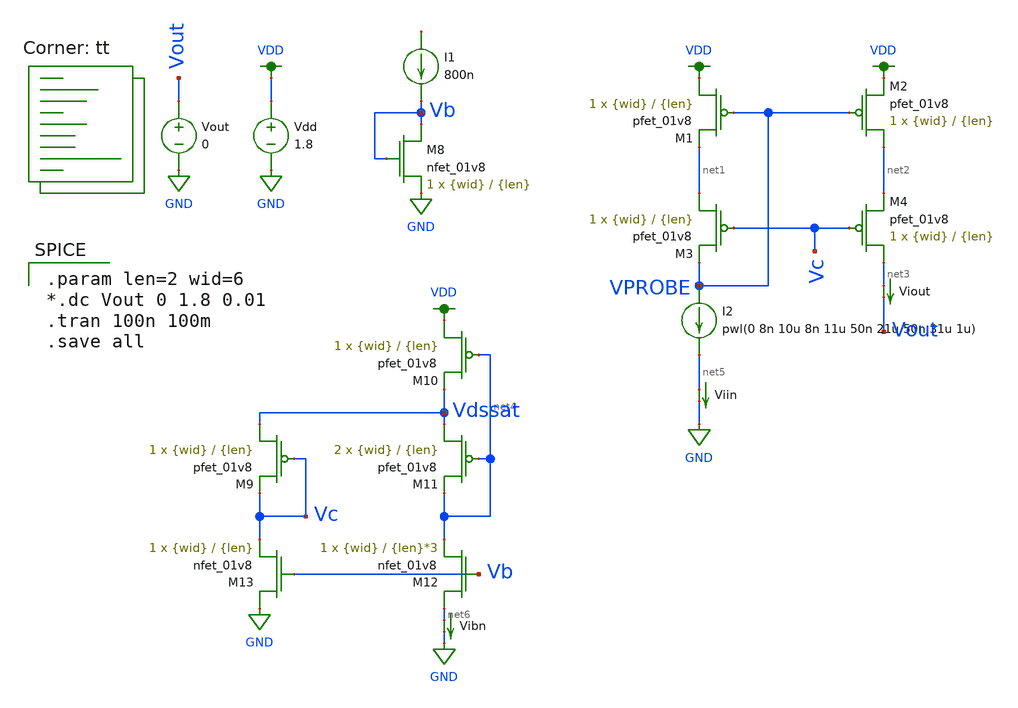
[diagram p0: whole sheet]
** sch_path: mp3/mirror_v2_tb.sch
**.subckt mirror_v2_tb
XM1 VDD VPROBE net1 VDD sky130_fd_pr__pfet_01v8 L={len} W={wid} nf=1 ad='int((nf+1)/2) * W/nf * 0.29'
+ as='int((nf+2)/2) * W/nf * 0.29' pd='2*int((nf+1)/2) * (W/nf + 0.29)' ps='2*int((nf+2)/2) * (W/nf + 0.29)'
+ nrd='0.29 / W' nrs='0.29 / W' sa=0 sb=0 sd=0 mult=1 m=1
XM2 net2 VPROBE VDD VDD sky130_fd_pr__pfet_01v8 L={len} W={wid} nf=1 ad='int((nf+1)/2) * W/nf * 0.29'
+ as='int((nf+2)/2) * W/nf * 0.29' pd='2*int((nf+1)/2) * (W/nf + 0.29)' ps='2*int((nf+2)/2) * (W/nf + 0.29)'
+ nrd='0.29 / W' nrs='0.29 / W' sa=0 sb=0 sd=0 mult=1 m=1
XM3 net1 Vc VPROBE VDD sky130_fd_pr__pfet_01v8 L={len} W={wid} nf=1 ad='int((nf+1)/2) * W/nf * 0.29'
+ as='int((nf+2)/2) * W/nf * 0.29' pd='2*int((nf+1)/2) * (W/nf + 0.29)' ps='2*int((nf+2)/2) * (W/nf + 0.29)'
+ nrd='0.29 / W' nrs='0.29 / W' sa=0 sb=0 sd=0 mult=1 m=1
XM4 net3 Vc net2 VDD sky130_fd_pr__pfet_01v8 L={len} W={wid} nf=1 ad='int((nf+1)/2) * W/nf * 0.29' as='int((nf+2)/2) * W/nf * 0.29'
+ pd='2*int((nf+1)/2) * (W/nf + 0.29)' ps='2*int((nf+2)/2) * (W/nf + 0.29)' nrd='0.29 / W' nrs='0.29 / W'
+ sa=0 sb=0 sd=0 mult=1 m=1
XM8 Vb Vb GND GND sky130_fd_pr__nfet_01v8 L={len} W={wid} nf=1 ad='int((nf+1)/2) * W/nf * 0.29' as='int((nf+2)/2) * W/nf * 0.29'
+ pd='2*int((nf+1)/2) * (W/nf + 0.29)' ps='2*int((nf+2)/2) * (W/nf + 0.29)' nrd='0.29 / W' nrs='0.29 / W'
+ sa=0 sb=0 sd=0 mult=1 m=1
I1 net7 Vb 800n
I2 VPROBE net5 pwl(0 8n 10u 8n 11u 50n 21u 50n 31u 1u)
XM9 Vdssat Vc Vc VDD sky130_fd_pr__pfet_01v8 L={len} W={wid} nf=1 ad='int((nf+1)/2) * W/nf * 0.29' as='int((nf+2)/2) * W/nf * 0.29'
+ pd='2*int((nf+1)/2) * (W/nf + 0.29)' ps='2*int((nf+2)/2) * (W/nf + 0.29)' nrd='0.29 / W' nrs='0.29 / W'
+ sa=0 sb=0 sd=0 mult=1 m=1
XM10 VDD net4 Vdssat VDD sky130_fd_pr__pfet_01v8 L={len} W={wid} nf=1 ad='int((nf+1)/2) * W/nf * 0.29'
+ as='int((nf+2)/2) * W/nf * 0.29' pd='2*int((nf+1)/2) * (W/nf + 0.29)' ps='2*int((nf+2)/2) * (W/nf + 0.29)'
+ nrd='0.29 / W' nrs='0.29 / W' sa=0 sb=0 sd=0 mult=1 m=1
XM11 Vdssat net4 net4 VDD sky130_fd_pr__pfet_01v8 L={len} W={wid} nf=1 ad='int((nf+1)/2) * W/nf * 0.29'
+ as='int((nf+2)/2) * W/nf * 0.29' pd='2*int((nf+1)/2) * (W/nf + 0.29)' ps='2*int((nf+2)/2) * (W/nf + 0.29)'
+ nrd='0.29 / W' nrs='0.29 / W' sa=0 sb=0 sd=0 mult=2 m=2
XM12 net6 Vb net4 GND sky130_fd_pr__nfet_01v8 L={len}*3 W={wid} nf=1 ad='int((nf+1)/2) * W/nf * 0.29'
+ as='int((nf+2)/2) * W/nf * 0.29' pd='2*int((nf+1)/2) * (W/nf + 0.29)' ps='2*int((nf+2)/2) * (W/nf + 0.29)'
+ nrd='0.29 / W' nrs='0.29 / W' sa=0 sb=0 sd=0 mult=1 m=1
XM13 GND Vb Vc GND sky130_fd_pr__nfet_01v8 L={len} W={wid} nf=1 ad='int((nf+1)/2) * W/nf * 0.29' as='int((nf+2)/2) * W/nf * 0.29'
+ pd='2*int((nf+1)/2) * (W/nf + 0.29)' ps='2*int((nf+2)/2) * (W/nf + 0.29)' nrd='0.29 / W' nrs='0.29 / W'
+ sa=0 sb=0 sd=0 mult=1 m=1
Vdd VDD GND 1.8
Viin net5 GND 0
.save i(viin)
Vibn net6 GND 0
.save i(vibn)
Vout Vout GND 0
Viout net3 Vout 0
.save i(viout)
**** begin user architecture code

.param len=2 wid=6
*.dc Vout 0 1.8 0.01
.tran 100n 100m
.save all


.lib $::SKYWATER_MODELS/sky130.lib.spice tt
**** end user architecture code
**.ends
.GLOBAL GND
.GLOBAL VDD
.end
